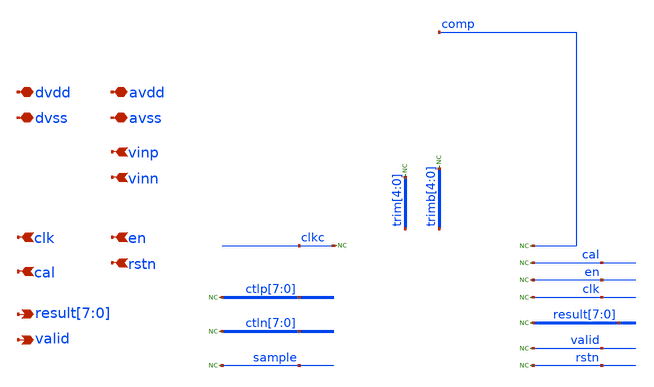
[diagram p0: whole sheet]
** sch_path: xschem/sar/SAR_POSTLAYOUT/sar.sch
**.subckt sar avss avdd dvss dvdd vinp vinn
*+ result[7],result[6],result[5],result[4],result[3],result[2],result[1],result[0] clk en valid cal rstn
*.iopin avss
*.iopin avdd
*.iopin dvss
*.iopin dvdd
*.ipin vinp
*.ipin vinn
*.opin result[7],result[6],result[5],result[4],result[3],result[2],result[1],result[0]
*.ipin clk
*.ipin en
*.opin valid
*.ipin cal
*.ipin rstn
* noconn comp
* noconn sample
* noconn ctln[7:0]
* noconn ctlp[7:0]
* noconn trim[4:0]
* noconn trimb[4:0]
* noconn result[7:0]
* noconn valid
* noconn clkc
* noconn clk
* noconn en
* noconn cal
* noconn rstn
**** begin user architecture code

*.include $::DESIGN_PATH/sar/control/cmos_cells_digital.sp
*.include $::DESIGN_PATH/sar/control/sar_logic.sp
*.include $::DESIGN_PATH/sar/control/sar_logic_sky.sp
.include $::DESIGN_PATH/sar/SAR_POSTLAYOUT/user_analog_project_wrapper.spice



**Xuut dclk drstn den dcomp dcal dvalid dres0 dres1 dres2 dres3 dres4 dres5 dres6 dres7 dsamp dctlp0
*+ dctlp1 dctlp2 dctlp3 dctlp4 dctlp5 dctlp6 dctlp7 dctln0 dctln1 dctln2 dctln3 dctln4 dctln5 dctln6 dctln7
*+ dtrim0 dtrim1 dtrim2 dtrim3 dtrim4 dtrimb0 dtrimb1 dtrimb2 dtrimb3 dtrimb4 dclkc sar_logic

.model adc_buff adc_bridge(in_low = 0.2 in_high=0.8)
.model dac_buff dac_bridge(out_high = 1.2)

Aad [clk rstn en comp cal] [dclk drstn den dcomp dcal] adc_buff
Ada [dctlp0 dctlp1 dctlp2 dctlp3 dctlp4 dctlp5 dctlp6 dctlp7 dctln0 dctln1 dctln2 dctln3 dctln4
+ dctln5 dctln6 dctln7 dres0 dres1 dres2 dres3 dres4 dres5 dres6 dres7 dsamp dclkc] [ctlp_0_ ctlp_1_ ctlp_2_
+ ctlp_3_ ctlp_4_ ctlp_5_ ctlp_6_ ctlp_7_ ctln_0_ ctln_1_ ctln_2_ ctln_3_ ctln_4_ ctln_5_ ctln_6_ ctln_7_
+ res0 res1 res2 res3 res4 res5 res6 res7 sample clkc] dac_buff
Ada2 [dtrim4 dtrim3 dtrim2 dtrim1 dtrim0 dtrimb4 dtrimb3 dtrimb2 dtrimb1 dtrimb0] [trim_4_ trim_3_
+ trim_2_ trim_1_ trim_0_ trimb_4_ trimb_3_ trimb_2_ trimb_1_ trimb_0_ ] dac_buff


xsar dcomp dctln1 dctln0 dctlp1 dctlp0 dctln7 dctln6 dctln5 dctln4 dctln3 dctln2 dtrim4  dtrim1
+ dtrim0 dtrim2 dtrim3 dtrimb3 dtrimb2 dtrimb0 dtrimb1 dtrimb4 dctlp2 dctlp3 dctlp4 dctlp5  dctlp6 dctlp7
+ dclkc dres7 dres6 dres5 dres4 drstn dres3 dres2 dres1 dres0  dvalid dcal den dclk vinp vinn dvdd avdd
+ dvss SAR


**** end user architecture code
**.ends
.end
